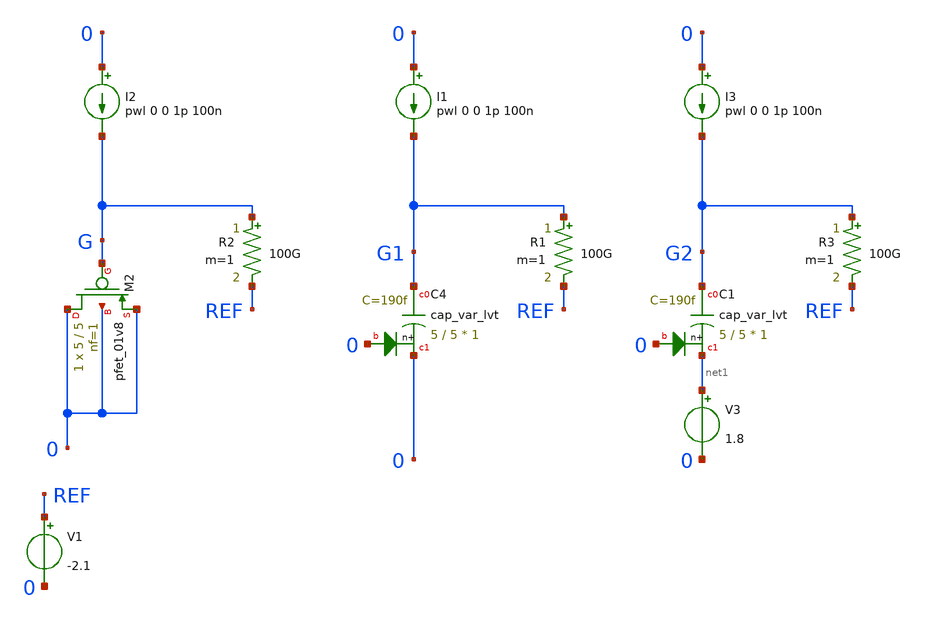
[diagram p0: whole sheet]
** sch_path: sky130A/xschem_libs/sky130_tests_ase/test_varactor/schematic/test_varactor.sch
* Copyright 2021 Stefan Frederik Schippers
* Licensed under the Apache License, Version 2.0 (the "License");
* you may not use this file except in compliance with the License.
* You may obtain a copy of the License at
* https://www.apache.org/licenses/LICENSE-2.0
* Unless required by applicable law or agreed to in writing, software
* distributed under the License is distributed on an "AS IS" BASIS,
* WITHOUT WARRANTIES OR CONDITIONS OF ANY KIND, either express or implied.
* See the License for the specific language governing permissions and
* limitations under the License.
**.subckt test_varactor
I1 0 G1 pwl 0 0 1p 100n
R1 G1 REF 100G m=1
I2 0 G pwl 0 0 1p 100n
R2 G REF 100G m=1
V1 REF 0 -2.1
XC4 G1 0 0 sky130_fd_pr__cap_var_lvt W=5 L=5 VM=1 m=1
XM2 0 G 0 0 sky130_fd_pr__pfet_01v8 L=5 W=5 nf=1 ad='int((nf+1)/2) * W/nf * 0.29' as='int((nf+2)/2) * W/nf * 0.29'
+ pd='2*int((nf+1)/2) * (W/nf + 0.29)' ps='2*int((nf+2)/2) * (W/nf + 0.29)' nrd='0.29 / W' nrs='0.29 / W'
+ sa=0 sb=0 sd=0 mult=1 m=1
I3 0 G2 pwl 0 0 1p 100n
R3 G2 REF 100G m=1
XC1 G2 net1 0 sky130_fd_pr__cap_var_lvt W=5 L=5 VM=1 m=1
V3 net1 0 1.8
**.ends
.end
